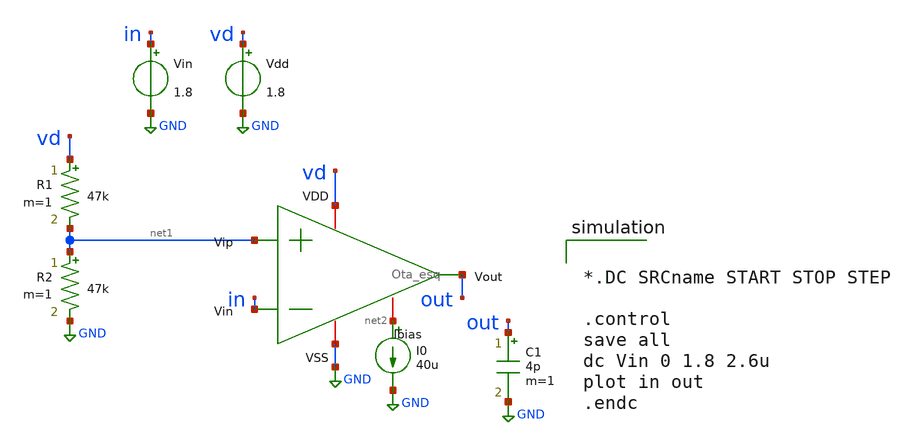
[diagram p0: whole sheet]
** sch_path: xschem/ota-tb-dc.sch
**.subckt ota-tb-dc
x1 vd in net1 out net2 GND Ota_esq
R1 vd net1 47k m=1
R2 net1 GND 47k m=1
Vin in GND 1.8
Vdd vd GND 1.8
I0 net2 GND 40u
C1 out GND 4p m=1
**** begin user architecture code


*.DC SRCname START STOP STEP

.control
save all
dc Vin 0 1.8 2.6u
plot in out
.endc




** opencircuitdesign pdks install
.lib $::SKYWATER_MODELS/sky130.lib.spice tt_mm


**** end user architecture code
**.ends

* expanding   symbol:  /foss/designs/ota-edson/Ota_esq.sym # of pins=6
** sym_path: /foss/designs/ota-edson/Ota_esq.sym
** sch_path: /foss/designs/ota-edson/Ota_esq.sch
.subckt Ota_esq VDD Vin Vip Vout Ibias VSS
*.ipin Vin
*.ipin Vip
*.iopin VDD
*.iopin VSS
*.iopin Ibias
*.opin Vout
XM1 net1 Vin net3 net3 sky130_fd_pr__pfet_01v8 L=0.25 W=2.899 nf=1 ad='int((nf+1)/2) * W/nf * 0.29' as='int((nf+2)/2) * W/nf * 0.29'
+ pd='2*int((nf+1)/2) * (W/nf + 0.29)' ps='2*int((nf+2)/2) * (W/nf + 0.29)' nrd='0.29 / W' nrs='0.29 / W'
+ sa=0 sb=0 sd=0 mult=1 m=1
XM2 net2 Vip net3 net3 sky130_fd_pr__pfet_01v8 L=0.25 W=2.899 nf=1 ad='int((nf+1)/2) * W/nf * 0.29' as='int((nf+2)/2) * W/nf * 0.29'
+ pd='2*int((nf+1)/2) * (W/nf + 0.29)' ps='2*int((nf+2)/2) * (W/nf + 0.29)' nrd='0.29 / W' nrs='0.29 / W'
+ sa=0 sb=0 sd=0 mult=1 m=1
XM3 net1 net1 VSS VSS sky130_fd_pr__nfet_01v8 L=0.25 W=0.667 nf=1 ad='int((nf+1)/2) * W/nf * 0.29' as='int((nf+2)/2) * W/nf * 0.29'
+ pd='2*int((nf+1)/2) * (W/nf + 0.29)' ps='2*int((nf+2)/2) * (W/nf + 0.29)' nrd='0.29 / W' nrs='0.29 / W'
+ sa=0 sb=0 sd=0 mult=1 m=1
XM4 net2 net1 VSS VSS sky130_fd_pr__nfet_01v8 L=0.25 W=0.667 nf=1 ad='int((nf+1)/2) * W/nf * 0.29' as='int((nf+2)/2) * W/nf * 0.29'
+ pd='2*int((nf+1)/2) * (W/nf + 0.29)' ps='2*int((nf+2)/2) * (W/nf + 0.29)' nrd='0.29 / W' nrs='0.29 / W'
+ sa=0 sb=0 sd=0 mult=1 m=1
XM5 net3 Ibias VDD VDD sky130_fd_pr__pfet_01v8 L=0.25 W=3.333 nf=1 ad='int((nf+1)/2) * W/nf * 0.29' as='int((nf+2)/2) * W/nf * 0.29'
+ pd='2*int((nf+1)/2) * (W/nf + 0.29)' ps='2*int((nf+2)/2) * (W/nf + 0.29)' nrd='0.29 / W' nrs='0.29 / W'
+ sa=0 sb=0 sd=0 mult=1 m=1
XM8 Ibias Ibias VDD VDD sky130_fd_pr__pfet_01v8 L=0.25 W=3.333 nf=1 ad='int((nf+1)/2) * W/nf * 0.29'
+ as='int((nf+2)/2) * W/nf * 0.29' pd='2*int((nf+1)/2) * (W/nf + 0.29)' ps='2*int((nf+2)/2) * (W/nf + 0.29)'
+ nrd='0.29 / W' nrs='0.29 / W' sa=0 sb=0 sd=0 mult=1 m=1
XM6 Vout Ibias VDD VDD sky130_fd_pr__pfet_01v8 L=0.25 W=17.279 nf=1 ad='int((nf+1)/2) * W/nf * 0.29'
+ as='int((nf+2)/2) * W/nf * 0.29' pd='2*int((nf+1)/2) * (W/nf + 0.29)' ps='2*int((nf+2)/2) * (W/nf + 0.29)'
+ nrd='0.29 / W' nrs='0.29 / W' sa=0 sb=0 sd=0 mult=1 m=1
XM7 Vout net2 VSS VSS sky130_fd_pr__nfet_01v8 L=0.25 W=6.192 nf=1 ad='int((nf+1)/2) * W/nf * 0.29' as='int((nf+2)/2) * W/nf * 0.29'
+ pd='2*int((nf+1)/2) * (W/nf + 0.29)' ps='2*int((nf+2)/2) * (W/nf + 0.29)' nrd='0.29 / W' nrs='0.29 / W'
+ sa=0 sb=0 sd=0 mult=1 m=1
XC1 net2 Vout sky130_fd_pr__cap_mim_m3_1 W=23 L=23 MF=1 m=1
.ends

.GLOBAL GND
.end
